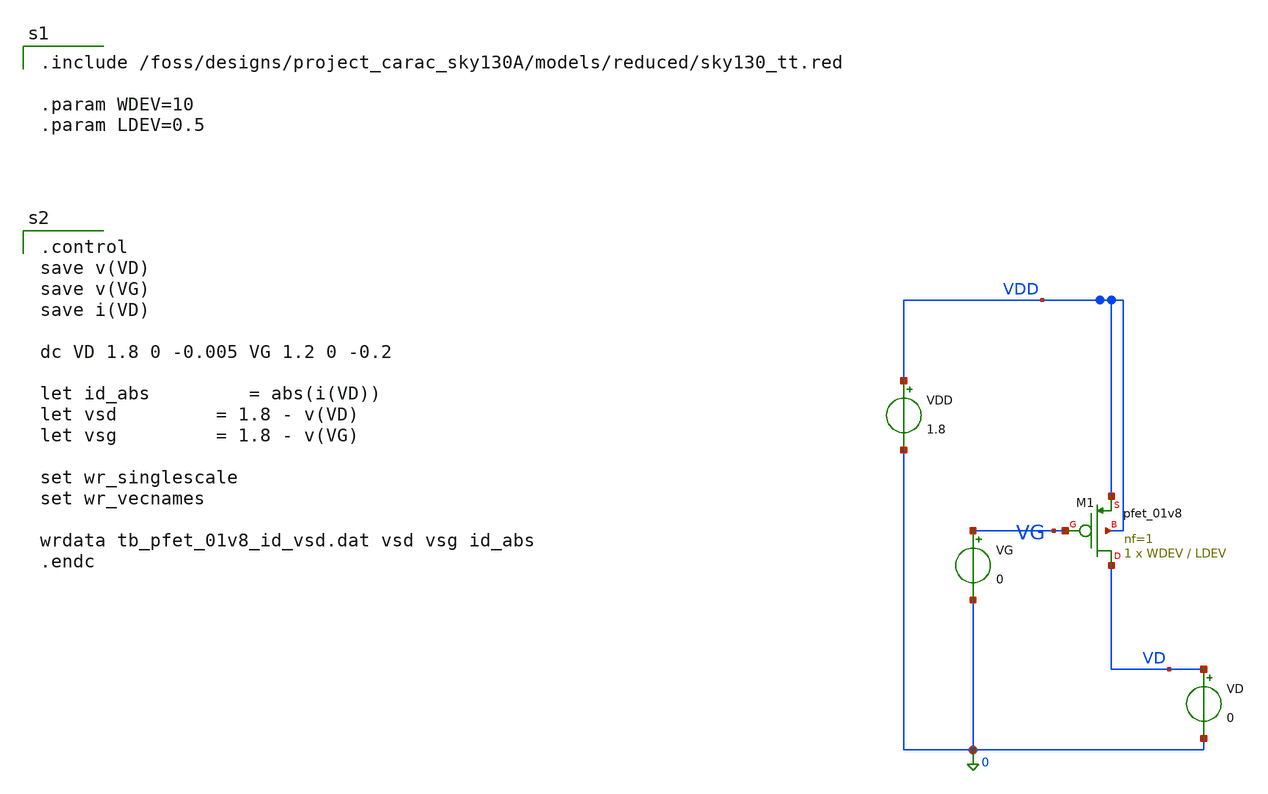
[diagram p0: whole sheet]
** sch_path: dfii/project_carac_sky130A_sim/tb_pfet_01v8_id_vsd.sch
* Copyright 2021 Stefan Frederik Schippers
* Licensed under the Apache License, Version 2.0 (the "License");
* you may not use this file except in compliance with the License.
* You may obtain a copy of the License at
* https://www.apache.org/licenses/LICENSE-2.0
* Unless required by applicable law or agreed to in writing, software
* distributed under the License is distributed on an "AS IS" BASIS,
* WITHOUT WARRANTIES OR CONDITIONS OF ANY KIND, either express or implied.
* See the License for the specific language governing permissions and
* limitations under the License.

.include /foss/designs/project_carac_sky130A/models/reduced/sky130_tt.red

.param WDEV=10
.param LDEV=0.5



**.subckt tb_pfet_01v8_id_vsd
VG VG 0 0
VD VD 0 0
.save i(vd)
XM1 VD VG VDD VDD sky130_fd_pr__pfet_01v8 L=LDEV W=WDEV nf=1 ad='int((1 + 1)/2) * WDEV / 1 * 0.29' as='int((1 + 2)/2) * WDEV / 1 * 0.29'
+ pd='2*int((1 + 1)/2) * (WDEV / 1 + 0.29)' ps='2*int((1 + 2)/2) * (WDEV / 1 + 0.29)' nrd='0.29 / WDEV '
+ nrs='0.29 / WDEV ' sa=0 sb=0 sd=0 mult=1 m=1
VDD VDD 0 1.8
**.ends
**** begin user architecture code

.control
save v(VD)
save v(VG)
save i(VD)

dc VD 1.8 0 -0.005 VG 1.2 0 -0.2

let id_abs 		= abs(i(VD))
let vsd 		= 1.8 - v(VD)
let vsg 		= 1.8 - v(VG)

set wr_singlescale
set wr_vecnames

wrdata tb_pfet_01v8_id_vsd.dat vsd vsg id_abs
.endc

**** end user architecture code
.end
